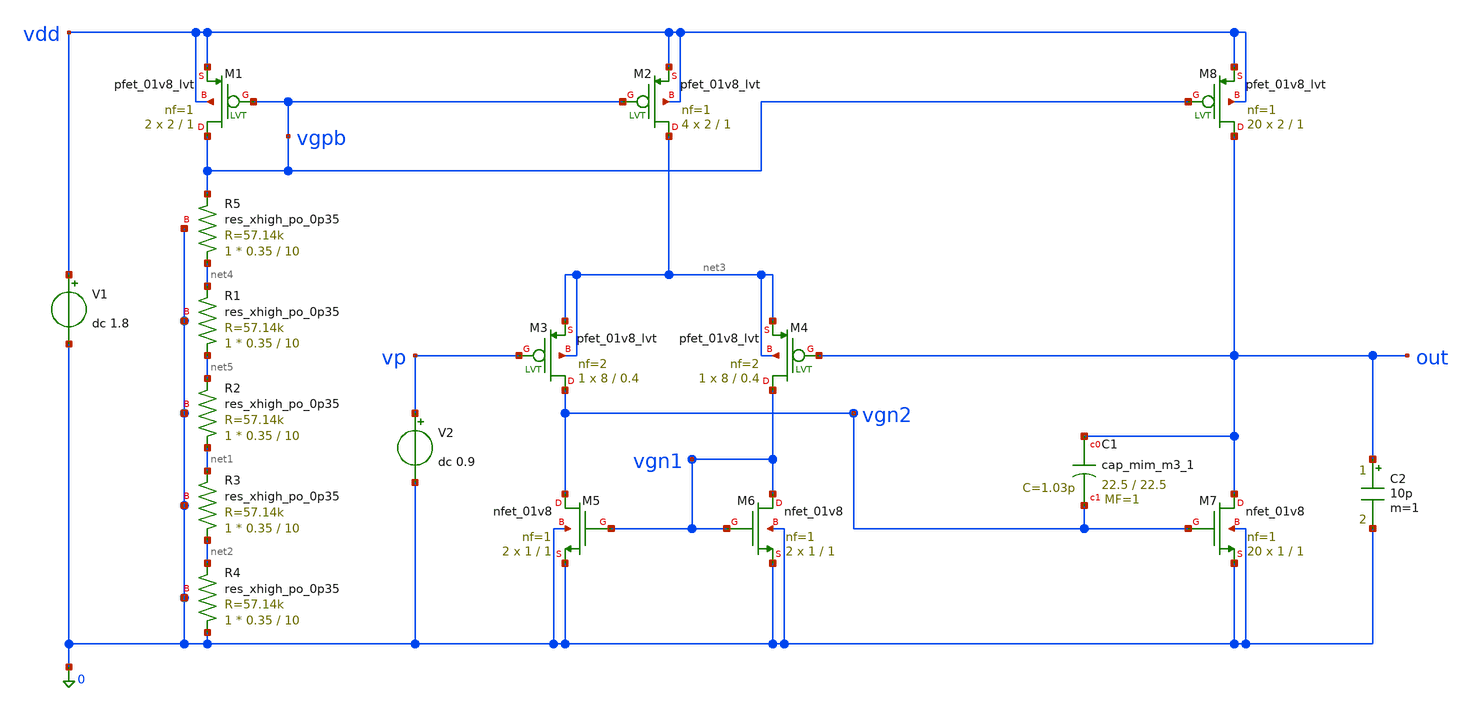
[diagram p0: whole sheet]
** sch_path: example_sch/opamp_dc.sch
**.subckt opamp_dc
XR2 net1 net5 0 sky130_fd_pr__res_xhigh_po_0p35 L=10 mult=1 m=1
XR3 net2 net1 0 sky130_fd_pr__res_xhigh_po_0p35 L=10 mult=1 m=1
XR4 0 net2 0 sky130_fd_pr__res_xhigh_po_0p35 L=10 mult=1 m=1
V1 vdd 0 dc 1.8
V2 vp 0 dc 0.9
XM5 vgn2 vgn1 0 0 sky130_fd_pr__nfet_01v8 L=1 W=1 nf=1 ad='int((nf+1)/2) * W/nf * 0.29' as='int((nf+2)/2) * W/nf * 0.29'
+ pd='2*int((nf+1)/2) * (W/nf + 0.29)' ps='2*int((nf+2)/2) * (W/nf + 0.29)' nrd='0.29 / W' nrs='0.29 / W'
+ sa=0 sb=0 sd=0 mult=2 m=2
XM6 vgn1 vgn1 0 0 sky130_fd_pr__nfet_01v8 L=1 W=1 nf=1 ad='int((nf+1)/2) * W/nf * 0.29' as='int((nf+2)/2) * W/nf * 0.29'
+ pd='2*int((nf+1)/2) * (W/nf + 0.29)' ps='2*int((nf+2)/2) * (W/nf + 0.29)' nrd='0.29 / W' nrs='0.29 / W'
+ sa=0 sb=0 sd=0 mult=2 m=2
XM7 out vgn2 0 0 sky130_fd_pr__nfet_01v8 L=1 W=1 nf=1 ad='int((nf+1)/2) * W/nf * 0.29' as='int((nf+2)/2) * W/nf * 0.29'
+ pd='2*int((nf+1)/2) * (W/nf + 0.29)' ps='2*int((nf+2)/2) * (W/nf + 0.29)' nrd='0.29 / W' nrs='0.29 / W'
+ sa=0 sb=0 sd=0 mult=20 m=20
XR1 net5 net4 0 sky130_fd_pr__res_xhigh_po_0p35 L=10 mult=1 m=1
XR5 net4 vgpb 0 sky130_fd_pr__res_xhigh_po_0p35 L=10 mult=1 m=1
XM1 vgpb vgpb vdd vdd sky130_fd_pr__pfet_01v8_lvt L=1 W=2 nf=1 ad='int((nf+1)/2) * W/nf * 0.29' as='int((nf+2)/2) * W/nf * 0.29'
+ pd='2*int((nf+1)/2) * (W/nf + 0.29)' ps='2*int((nf+2)/2) * (W/nf + 0.29)' nrd='0.29 / W' nrs='0.29 / W'
+ sa=0 sb=0 sd=0 mult=2 m=2
XM2 net3 vgpb vdd vdd sky130_fd_pr__pfet_01v8_lvt L=1 W=2 nf=1 ad='int((nf+1)/2) * W/nf * 0.29' as='int((nf+2)/2) * W/nf * 0.29'
+ pd='2*int((nf+1)/2) * (W/nf + 0.29)' ps='2*int((nf+2)/2) * (W/nf + 0.29)' nrd='0.29 / W' nrs='0.29 / W'
+ sa=0 sb=0 sd=0 mult=4 m=4
XM8 out vgpb vdd vdd sky130_fd_pr__pfet_01v8_lvt L=1 W=2 nf=1 ad='int((nf+1)/2) * W/nf * 0.29' as='int((nf+2)/2) * W/nf * 0.29'
+ pd='2*int((nf+1)/2) * (W/nf + 0.29)' ps='2*int((nf+2)/2) * (W/nf + 0.29)' nrd='0.29 / W' nrs='0.29 / W'
+ sa=0 sb=0 sd=0 mult=20 m=20
XM3 vgn2 vp net3 net3 sky130_fd_pr__pfet_01v8_lvt L=0.4 W=8 nf=2 ad='int((nf+1)/2) * W/nf * 0.29' as='int((nf+2)/2) * W/nf * 0.29'
+ pd='2*int((nf+1)/2) * (W/nf + 0.29)' ps='2*int((nf+2)/2) * (W/nf + 0.29)' nrd='0.29 / W' nrs='0.29 / W'
+ sa=0 sb=0 sd=0 mult=1 m=1
XM4 vgn1 out net3 net3 sky130_fd_pr__pfet_01v8_lvt L=0.4 W=8 nf=2 ad='int((nf+1)/2) * W/nf * 0.29' as='int((nf+2)/2) * W/nf * 0.29'
+ pd='2*int((nf+1)/2) * (W/nf + 0.29)' ps='2*int((nf+2)/2) * (W/nf + 0.29)' nrd='0.29 / W' nrs='0.29 / W'
+ sa=0 sb=0 sd=0 mult=1 m=1
XC1 out vgn2 sky130_fd_pr__cap_mim_m3_1 W=22.5 L=22.5 MF=1 m=1
C2 out 0 10p m=1
**** begin user architecture code

** opencircuitdesign pdks install
.lib $::SKYWATER_MODELS/sky130.lib.spice tt


**** end user architecture code
**.ends
**** begin user architecture code


*** Save all devices' currents ***
.options savecurrents

*** Save all voltages	and others ***
.save all
.save @m.xm3.msky130_fd_pr__pfet_01v8_lvt[gm]
.save @m.xm4.msky130_fd_pr__pfet_01v8_lvt[gm]
.save @m.xm7.msky130_fd_pr__nfet_01v8[gm]

**** Control statements for simulation ****
*   .control <-- start of control statement
*   op       <-- calculate operating point
*   show ... <-- print MOSFET OP in details
*   write    <-- write results into a RAW file
*   quit     <-- leave simulation
*   .endc    <-- end of control statement
********************************************
.control
op
show m : vgs : vth : vds : vdsat : gm : gds
write
quit
.endc


**** end user architecture code
.end
